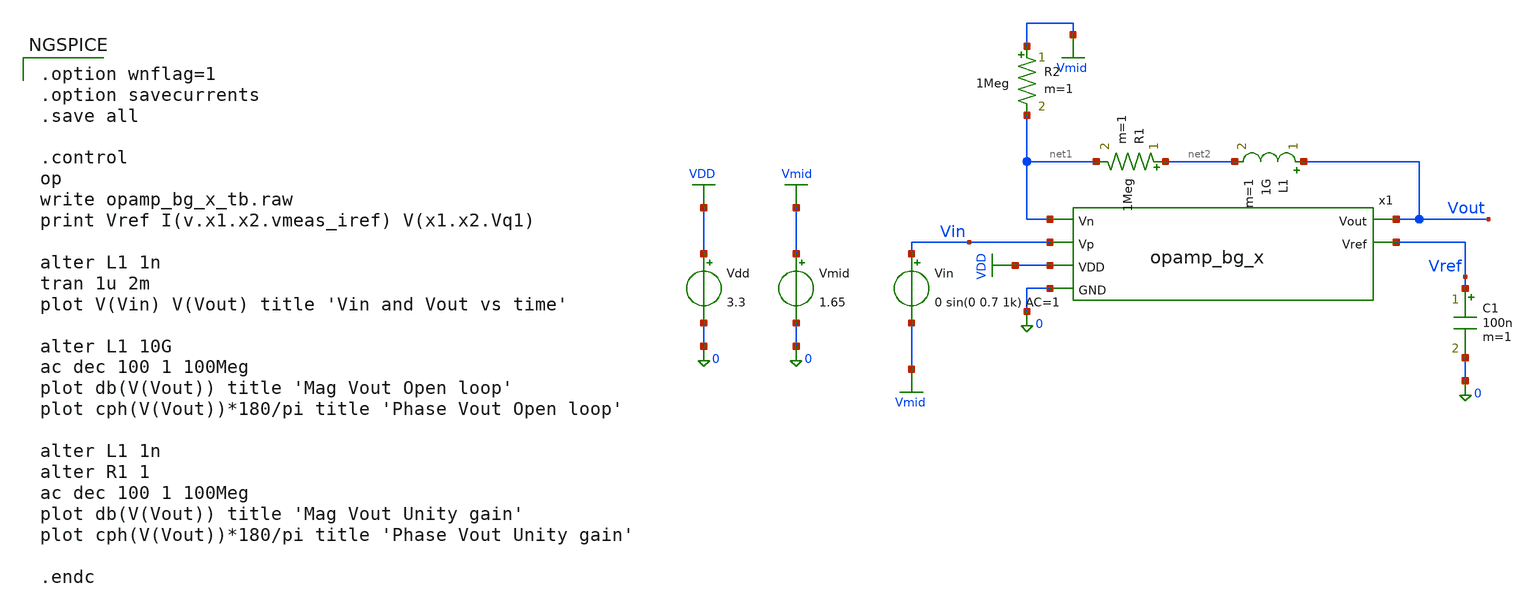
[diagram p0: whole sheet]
** sch_path: xschem/opamp_bg_x_tb.sch
**.subckt opamp_bg_x_tb
x1 Vref net1 Vout Vin VDD 0 opamp_bg_x
R1 net2 net1 1Meg m=1
L1 Vout net2 1G m=1
R2 Vmid net1 1Meg m=1
Vin Vin Vmid 0 sin(0 0.7 1k) AC=1
Vmid Vmid 0 1.65
Vdd VDD 0 3.3
C1 Vref 0 100n m=1
**** begin user architecture code

.option wnflag=1
.option savecurrents
.save all

.control
op
write opamp_bg_x_tb.raw
print Vref I(v.x1.x2.vmeas_iref) V(x1.x2.Vq1)

alter L1 1n
tran 1u 2m
plot V(Vin) V(Vout) title 'Vin and Vout vs time'

alter L1 10G
ac dec 100 1 100Meg
plot db(V(Vout)) title 'Mag Vout Open loop'
plot cph(V(Vout))*180/pi title 'Phase Vout Open loop'

alter L1 1n
alter R1 1
ac dec 100 1 100Meg
plot db(V(Vout)) title 'Mag Vout Unity gain'
plot cph(V(Vout))*180/pi title 'Phase Vout Unity gain'

.endc


** opencircuitdesign pdks install
.lib $::SKYWATER_MODELS/sky130.lib.spice tt

**** end user architecture code
**.ends

* expanding   symbol:  opamp_bg_x.sym # of pins=6
** sym_path: xschem/opamp_bg_x.sym
** sch_path: xschem/opamp_bg_x.sch
.subckt opamp_bg_x Vref Vn Vout Vp VDD GND
*.ipin Vn
*.opin Vout
*.opin Vref
*.ipin Vp
*.ipin VDD
*.ipin GND
x1 VDD Vref GND bandgap_x
x2 VDD Vp Vn Vout Vref GND opamp_x
.ends


* expanding   symbol:  /home/bbarkey/Documents/ECE_5120/homework_05/xschem/bandgap_x.sym # of pins=3
** sym_path: xschem/bandgap_x.sym
** sch_path: xschem/bandgap_x.sch
.subckt bandgap_x VDD Vref GND
*.opin Vref
*.ipin GND
*.ipin VDD
XM2 Vg3 Vg2 net1 net1 sky130_fd_pr__pfet_g5v0d10v5 L=1 W=20 nf=1 ad='int((1 + 1)/2) * 20 / 1 * 0.29'
+ as='int((1 + 2)/2) * 20 / 1 * 0.29' pd='2*int((1 + 1)/2) * (20 / 1 + 0.29)' ps='2*int((1 + 2)/2) * (20 / 1 + 0.29)'
+ nrd='0.29 / 20 ' nrs='0.29 / 20 ' sa=0 sb=0 sd=0 mult=1 m=1
XM1 Vg10 Vg1 net1 net1 sky130_fd_pr__pfet_g5v0d10v5 L=1 W=20 nf=1 ad='int((1 + 1)/2) * 20 / 1 * 0.29'
+ as='int((1 + 2)/2) * 20 / 1 * 0.29' pd='2*int((1 + 1)/2) * (20 / 1 + 0.29)' ps='2*int((1 + 2)/2) * (20 / 1 + 0.29)'
+ nrd='0.29 / 20 ' nrs='0.29 / 20 ' sa=0 sb=0 sd=0 mult=1 m=1
XM3 Vg10 Vg3 GND GND sky130_fd_pr__nfet_g5v0d10v5 L=1 W=20 nf=1 ad='int((1 + 1)/2) * 20 / 1 * 0.29' as='int((1 + 2)/2) * 20 / 1 * 0.29'
+ pd='2*int((1 + 1)/2) * (20 / 1 + 0.29)' ps='2*int((1 + 2)/2) * (20 / 1 + 0.29)' nrd='0.29 / 20 ' nrs='0.29 / 20 '
+ sa=0 sb=0 sd=0 mult=1 m=1
XM4 Vg3 Vg3 GND GND sky130_fd_pr__nfet_g5v0d10v5 L=1 W=20 nf=1 ad='int((1 + 1)/2) * 20 / 1 * 0.29' as='int((1 + 2)/2) * 20 / 1 * 0.29'
+ pd='2*int((1 + 1)/2) * (20 / 1 + 0.29)' ps='2*int((1 + 2)/2) * (20 / 1 + 0.29)' nrd='0.29 / 20 ' nrs='0.29 / 20 '
+ sa=0 sb=0 sd=0 mult=1 m=1
XM5 Vg5 Vg5 VDD VDD sky130_fd_pr__pfet_g5v0d10v5 L=1 W=1 nf=1 ad='int((1 + 1)/2) * 1 / 1 * 0.29' as='int((1 + 2)/2) * 1 / 1 * 0.29'
+ pd='2*int((1 + 1)/2) * (1 / 1 + 0.29)' ps='2*int((1 + 2)/2) * (1 / 1 + 0.29)' nrd='0.29 / 1 ' nrs='0.29 / 1 '
+ sa=0 sb=0 sd=0 mult=1 m=1
XM6 Vg5 Vref Vs5 GND sky130_fd_pr__nfet_g5v0d10v5 L=1 W=5 nf=1 ad='int((1 + 1)/2) * 5 / 1 * 0.29' as='int((1 + 2)/2) * 5 / 1 * 0.29'
+ pd='2*int((1 + 1)/2) * (5 / 1 + 0.29)' ps='2*int((1 + 2)/2) * (5 / 1 + 0.29)' nrd='0.29 / 5 ' nrs='0.29 / 5 '
+ sa=0 sb=0 sd=0 mult=1 m=1
XM7a Vg12 Vg12 net3 GND sky130_fd_pr__nfet_g5v0d10v5 L=10 W=0.5 nf=1 ad='int((1 + 1)/2) * 0.5 / 1 * 0.29'
+ as='int((1 + 2)/2) * 0.5 / 1 * 0.29' pd='2*int((1 + 1)/2) * (0.5 / 1 + 0.29)' ps='2*int((1 + 2)/2) * (0.5 / 1 + 0.29)'
+ nrd='0.29 / 0.5 ' nrs='0.29 / 0.5 ' sa=0 sb=0 sd=0 mult=1 m=1
XM8 Vg12 Vg5 VDD VDD sky130_fd_pr__pfet_g5v0d10v5 L=1 W=1 nf=1 ad='int((1 + 1)/2) * 1 / 1 * 0.29' as='int((1 + 2)/2) * 1 / 1 * 0.29'
+ pd='2*int((1 + 1)/2) * (1 / 1 + 0.29)' ps='2*int((1 + 2)/2) * (1 / 1 + 0.29)' nrd='0.29 / 1 ' nrs='0.29 / 1 '
+ sa=0 sb=0 sd=0 mult=1 m=1
XM9 Vg12 Vref net2 GND sky130_fd_pr__nfet_g5v0d10v5 L=1 W=20 nf=1 ad='int((1 + 1)/2) * 20 / 1 * 0.29'
+ as='int((1 + 2)/2) * 20 / 1 * 0.29' pd='2*int((1 + 1)/2) * (20 / 1 + 0.29)' ps='2*int((1 + 2)/2) * (20 / 1 + 0.29)'
+ nrd='0.29 / 20 ' nrs='0.29 / 20 ' sa=0 sb=0 sd=0 mult=1 m=1
XM10 net2 Vg10 GND GND sky130_fd_pr__nfet_g5v0d10v5 L=1 W=20 nf=1 ad='int((1 + 1)/2) * 20 / 1 * 0.29'
+ as='int((1 + 2)/2) * 20 / 1 * 0.29' pd='2*int((1 + 1)/2) * (20 / 1 + 0.29)' ps='2*int((1 + 2)/2) * (20 / 1 + 0.29)'
+ nrd='0.29 / 20 ' nrs='0.29 / 20 ' sa=0 sb=0 sd=0 mult=1 m=1
XM11 net1 Vg5 VDD VDD sky130_fd_pr__pfet_g5v0d10v5 L=1 W=1 nf=1 ad='int((1 + 1)/2) * 1 / 1 * 0.29' as='int((1 + 2)/2) * 1 / 1 * 0.29'
+ pd='2*int((1 + 1)/2) * (1 / 1 + 0.29)' ps='2*int((1 + 2)/2) * (1 / 1 + 0.29)' nrd='0.29 / 1 ' nrs='0.29 / 1 '
+ sa=0 sb=0 sd=0 mult=1 m=1
XM12 Vref Vg12 VDD VDD sky130_fd_pr__pfet_g5v0d10v5 L=0.5 W=20 nf=1 ad='int((1 + 1)/2) * 20 / 1 * 0.29'
+ as='int((1 + 2)/2) * 20 / 1 * 0.29' pd='2*int((1 + 1)/2) * (20 / 1 + 0.29)' ps='2*int((1 + 2)/2) * (20 / 1 + 0.29)'
+ nrd='0.29 / 20 ' nrs='0.29 / 20 ' sa=0 sb=0 sd=0 mult=1 m=1
XR1 Vg2 Vref GND sky130_fd_pr__res_high_po_0p35 L=21.3 mult=1 m=1
XR2 Vg1 Vref GND sky130_fd_pr__res_high_po_0p35 L=21.3 mult=1 m=1
XR3 Ve1 Vg1 GND sky130_fd_pr__res_high_po_0p35 L=3 mult=1 m=1
XR4 GND Vs5 GND sky130_fd_pr__res_high_po_0p35 L=47.02 mult=1 m=1
XQ1 GND GND Ve1 sky130_fd_pr__pnp_05v5_W3p40L3p40 m=24
XQ2 GND GND Vg2 sky130_fd_pr__pnp_05v5_W3p40L3p40 m=1
XM7b net3 Vg12 net4 GND sky130_fd_pr__nfet_g5v0d10v5 L=10 W=0.5 nf=1 ad='int((1 + 1)/2) * 0.5 / 1 * 0.29'
+ as='int((1 + 2)/2) * 0.5 / 1 * 0.29' pd='2*int((1 + 1)/2) * (0.5 / 1 + 0.29)' ps='2*int((1 + 2)/2) * (0.5 / 1 + 0.29)'
+ nrd='0.29 / 0.5 ' nrs='0.29 / 0.5 ' sa=0 sb=0 sd=0 mult=1 m=1
XM7c net4 Vg12 net5 GND sky130_fd_pr__nfet_g5v0d10v5 L=10 W=0.5 nf=1 ad='int((1 + 1)/2) * 0.5 / 1 * 0.29'
+ as='int((1 + 2)/2) * 0.5 / 1 * 0.29' pd='2*int((1 + 1)/2) * (0.5 / 1 + 0.29)' ps='2*int((1 + 2)/2) * (0.5 / 1 + 0.29)'
+ nrd='0.29 / 0.5 ' nrs='0.29 / 0.5 ' sa=0 sb=0 sd=0 mult=1 m=1
XM7d net5 Vg12 net6 GND sky130_fd_pr__nfet_g5v0d10v5 L=10 W=0.5 nf=1 ad='int((1 + 1)/2) * 0.5 / 1 * 0.29'
+ as='int((1 + 2)/2) * 0.5 / 1 * 0.29' pd='2*int((1 + 1)/2) * (0.5 / 1 + 0.29)' ps='2*int((1 + 2)/2) * (0.5 / 1 + 0.29)'
+ nrd='0.29 / 0.5 ' nrs='0.29 / 0.5 ' sa=0 sb=0 sd=0 mult=1 m=1
XM7e net6 Vg12 net7 GND sky130_fd_pr__nfet_g5v0d10v5 L=10 W=0.5 nf=1 ad='int((1 + 1)/2) * 0.5 / 1 * 0.29'
+ as='int((1 + 2)/2) * 0.5 / 1 * 0.29' pd='2*int((1 + 1)/2) * (0.5 / 1 + 0.29)' ps='2*int((1 + 2)/2) * (0.5 / 1 + 0.29)'
+ nrd='0.29 / 0.5 ' nrs='0.29 / 0.5 ' sa=0 sb=0 sd=0 mult=1 m=1
XM7 net7 Vg12 net8 GND sky130_fd_pr__nfet_g5v0d10v5 L=10 W=0.5 nf=1 ad='int((1 + 1)/2) * 0.5 / 1 * 0.29'
+ as='int((1 + 2)/2) * 0.5 / 1 * 0.29' pd='2*int((1 + 1)/2) * (0.5 / 1 + 0.29)' ps='2*int((1 + 2)/2) * (0.5 / 1 + 0.29)'
+ nrd='0.29 / 0.5 ' nrs='0.29 / 0.5 ' sa=0 sb=0 sd=0 mult=1 m=1
XM13 net8 Vg12 net9 GND sky130_fd_pr__nfet_g5v0d10v5 L=10 W=0.5 nf=1 ad='int((1 + 1)/2) * 0.5 / 1 * 0.29'
+ as='int((1 + 2)/2) * 0.5 / 1 * 0.29' pd='2*int((1 + 1)/2) * (0.5 / 1 + 0.29)' ps='2*int((1 + 2)/2) * (0.5 / 1 + 0.29)'
+ nrd='0.29 / 0.5 ' nrs='0.29 / 0.5 ' sa=0 sb=0 sd=0 mult=1 m=1
XM14 net9 Vg12 net10 GND sky130_fd_pr__nfet_g5v0d10v5 L=10 W=0.5 nf=1 ad='int((1 + 1)/2) * 0.5 / 1 * 0.29'
+ as='int((1 + 2)/2) * 0.5 / 1 * 0.29' pd='2*int((1 + 1)/2) * (0.5 / 1 + 0.29)' ps='2*int((1 + 2)/2) * (0.5 / 1 + 0.29)'
+ nrd='0.29 / 0.5 ' nrs='0.29 / 0.5 ' sa=0 sb=0 sd=0 mult=1 m=1
XM15 net10 Vg12 net11 GND sky130_fd_pr__nfet_g5v0d10v5 L=10 W=0.5 nf=1 ad='int((1 + 1)/2) * 0.5 / 1 * 0.29'
+ as='int((1 + 2)/2) * 0.5 / 1 * 0.29' pd='2*int((1 + 1)/2) * (0.5 / 1 + 0.29)' ps='2*int((1 + 2)/2) * (0.5 / 1 + 0.29)'
+ nrd='0.29 / 0.5 ' nrs='0.29 / 0.5 ' sa=0 sb=0 sd=0 mult=1 m=1
XM16 net11 Vg12 GND GND sky130_fd_pr__nfet_g5v0d10v5 L=10 W=0.5 nf=1 ad='int((1 + 1)/2) * 0.5 / 1 * 0.29'
+ as='int((1 + 2)/2) * 0.5 / 1 * 0.29' pd='2*int((1 + 1)/2) * (0.5 / 1 + 0.29)' ps='2*int((1 + 2)/2) * (0.5 / 1 + 0.29)'
+ nrd='0.29 / 0.5 ' nrs='0.29 / 0.5 ' sa=0 sb=0 sd=0 mult=1 m=1
.ends


* expanding   symbol:  opamp_x.sym # of pins=6
** sym_path: xschem/opamp_x.sym
** sch_path: xschem/opamp_x.sch
.subckt opamp_x VDD Vp Vn Vout Vref GND
*.ipin Vref
*.ipin Vn
*.ipin Vp
*.opin Vout
*.ipin VDD
*.ipin GND
XM1 net3 net3 net1 GND sky130_fd_pr__nfet_g5v0d10v5 L=2 W=3.33 nf=1 ad='int((1 + 1)/2) * 3.33 / 1 * 0.29'
+ as='int((1 + 2)/2) * 3.33 / 1 * 0.29' pd='2*int((1 + 1)/2) * (3.33 / 1 + 0.29)' ps='2*int((1 + 2)/2) * (3.33 / 1 + 0.29)'
+ nrd='0.29 / 3.33 ' nrs='0.29 / 3.33 ' sa=0 sb=0 sd=0 mult=3 m=3
XM2 net1 net3 GND GND sky130_fd_pr__nfet_g5v0d10v5 L=5 W=5 nf=1 ad='int((1 + 1)/2) * 5 / 1 * 0.29' as='int((1 + 2)/2) * 5 / 1 * 0.29'
+ pd='2*int((1 + 1)/2) * (5 / 1 + 0.29)' ps='2*int((1 + 2)/2) * (5 / 1 + 0.29)' nrd='0.29 / 5 ' nrs='0.29 / 5 '
+ sa=0 sb=0 sd=0 mult=1 m=1
XM3 net2 net3 net4 GND sky130_fd_pr__nfet_g5v0d10v5 L=2 W=3.33 nf=1 ad='int((1 + 1)/2) * 3.33 / 1 * 0.29'
+ as='int((1 + 2)/2) * 3.33 / 1 * 0.29' pd='2*int((1 + 1)/2) * (3.33 / 1 + 0.29)' ps='2*int((1 + 2)/2) * (3.33 / 1 + 0.29)'
+ nrd='0.29 / 3.33 ' nrs='0.29 / 3.33 ' sa=0 sb=0 sd=0 mult=3 m=3
XM4 net4 net3 GND GND sky130_fd_pr__nfet_g5v0d10v5 L=5 W=5 nf=1 ad='int((1 + 1)/2) * 5 / 1 * 0.29' as='int((1 + 2)/2) * 5 / 1 * 0.29'
+ pd='2*int((1 + 1)/2) * (5 / 1 + 0.29)' ps='2*int((1 + 2)/2) * (5 / 1 + 0.29)' nrd='0.29 / 5 ' nrs='0.29 / 5 '
+ sa=0 sb=0 sd=0 mult=1 m=1
XM5 net5 net2 VDD VDD sky130_fd_pr__pfet_g5v0d10v5 L=1 W=3 nf=1 ad='int((1 + 1)/2) * 3 / 1 * 0.29' as='int((1 + 2)/2) * 3 / 1 * 0.29'
+ pd='2*int((1 + 1)/2) * (3 / 1 + 0.29)' ps='2*int((1 + 2)/2) * (3 / 1 + 0.29)' nrd='0.29 / 3 ' nrs='0.29 / 3 '
+ sa=0 sb=0 sd=0 mult=1 m=1
XM6 net2 net2 net5 VDD sky130_fd_pr__pfet_g5v0d10v5 L=1 W=10 nf=1 ad='int((1 + 1)/2) * 10 / 1 * 0.29'
+ as='int((1 + 2)/2) * 10 / 1 * 0.29' pd='2*int((1 + 1)/2) * (10 / 1 + 0.29)' ps='2*int((1 + 2)/2) * (10 / 1 + 0.29)'
+ nrd='0.29 / 10 ' nrs='0.29 / 10 ' sa=0 sb=0 sd=0 mult=1 m=1
XM7 net6 net2 VDD VDD sky130_fd_pr__pfet_g5v0d10v5 L=1 W=1 nf=1 ad='int((1 + 1)/2) * 1 / 1 * 0.29' as='int((1 + 2)/2) * 1 / 1 * 0.29'
+ pd='2*int((1 + 1)/2) * (1 / 1 + 0.29)' ps='2*int((1 + 2)/2) * (1 / 1 + 0.29)' nrd='0.29 / 1 ' nrs='0.29 / 1 '
+ sa=0 sb=0 sd=0 mult=3 m=3
XM8 net7 net2 net6 VDD sky130_fd_pr__pfet_g5v0d10v5 L=0.5 W=10 nf=1 ad='int((1 + 1)/2) * 10 / 1 * 0.29'
+ as='int((1 + 2)/2) * 10 / 1 * 0.29' pd='2*int((1 + 1)/2) * (10 / 1 + 0.29)' ps='2*int((1 + 2)/2) * (10 / 1 + 0.29)'
+ nrd='0.29 / 10 ' nrs='0.29 / 10 ' sa=0 sb=0 sd=0 mult=1 m=1
XM9 net13 Vp net7 VDD sky130_fd_pr__pfet_g5v0d10v5 L=3 W=20 nf=1 ad='int((1 + 1)/2) * 20 / 1 * 0.29'
+ as='int((1 + 2)/2) * 20 / 1 * 0.29' pd='2*int((1 + 1)/2) * (20 / 1 + 0.29)' ps='2*int((1 + 2)/2) * (20 / 1 + 0.29)'
+ nrd='0.29 / 20 ' nrs='0.29 / 20 ' sa=0 sb=0 sd=0 mult=10 m=10
XM10 net12 Vn net7 VDD sky130_fd_pr__pfet_g5v0d10v5 L=3 W=20 nf=1 ad='int((1 + 1)/2) * 20 / 1 * 0.29'
+ as='int((1 + 2)/2) * 20 / 1 * 0.29' pd='2*int((1 + 1)/2) * (20 / 1 + 0.29)' ps='2*int((1 + 2)/2) * (20 / 1 + 0.29)'
+ nrd='0.29 / 20 ' nrs='0.29 / 20 ' sa=0 sb=0 sd=0 mult=10 m=10
XM11 net10 net9 VDD VDD sky130_fd_pr__pfet_g5v0d10v5 L=0.5 W=2 nf=1 ad='int((1 + 1)/2) * 2 / 1 * 0.29'
+ as='int((1 + 2)/2) * 2 / 1 * 0.29' pd='2*int((1 + 1)/2) * (2 / 1 + 0.29)' ps='2*int((1 + 2)/2) * (2 / 1 + 0.29)'
+ nrd='0.29 / 2 ' nrs='0.29 / 2 ' sa=0 sb=0 sd=0 mult=5 m=5
XM12 net9 net9 net10 VDD sky130_fd_pr__pfet_g5v0d10v5 L=0.5 W=5 nf=1 ad='int((1 + 1)/2) * 5 / 1 * 0.29'
+ as='int((1 + 2)/2) * 5 / 1 * 0.29' pd='2*int((1 + 1)/2) * (5 / 1 + 0.29)' ps='2*int((1 + 2)/2) * (5 / 1 + 0.29)'
+ nrd='0.29 / 5 ' nrs='0.29 / 5 ' sa=0 sb=0 sd=0 mult=5 m=5
XM13 net11 net9 VDD VDD sky130_fd_pr__pfet_g5v0d10v5 L=0.5 W=2 nf=1 ad='int((1 + 1)/2) * 2 / 1 * 0.29'
+ as='int((1 + 2)/2) * 2 / 1 * 0.29' pd='2*int((1 + 1)/2) * (2 / 1 + 0.29)' ps='2*int((1 + 2)/2) * (2 / 1 + 0.29)'
+ nrd='0.29 / 2 ' nrs='0.29 / 2 ' sa=0 sb=0 sd=0 mult=5 m=5
XM14 net18 net9 net11 VDD sky130_fd_pr__pfet_g5v0d10v5 L=0.5 W=5 nf=1 ad='int((1 + 1)/2) * 5 / 1 * 0.29'
+ as='int((1 + 2)/2) * 5 / 1 * 0.29' pd='2*int((1 + 1)/2) * (5 / 1 + 0.29)' ps='2*int((1 + 2)/2) * (5 / 1 + 0.29)'
+ nrd='0.29 / 5 ' nrs='0.29 / 5 ' sa=0 sb=0 sd=0 mult=5 m=5
XM15 net9 net3 net12 GND sky130_fd_pr__nfet_g5v0d10v5 L=0.5 W=5 nf=1 ad='int((1 + 1)/2) * 5 / 1 * 0.29'
+ as='int((1 + 2)/2) * 5 / 1 * 0.29' pd='2*int((1 + 1)/2) * (5 / 1 + 0.29)' ps='2*int((1 + 2)/2) * (5 / 1 + 0.29)'
+ nrd='0.29 / 5 ' nrs='0.29 / 5 ' sa=0 sb=0 sd=0 mult=5 m=5
XM16 net12 net3 GND GND sky130_fd_pr__nfet_g5v0d10v5 L=0.5 W=1 nf=1 ad='int((1 + 1)/2) * 1 / 1 * 0.29'
+ as='int((1 + 2)/2) * 1 / 1 * 0.29' pd='2*int((1 + 1)/2) * (1 / 1 + 0.29)' ps='2*int((1 + 2)/2) * (1 / 1 + 0.29)'
+ nrd='0.29 / 1 ' nrs='0.29 / 1 ' sa=0 sb=0 sd=0 mult=1 m=1
XM17 net17 net3 net13 GND sky130_fd_pr__nfet_g5v0d10v5 L=0.5 W=5 nf=1 ad='int((1 + 1)/2) * 5 / 1 * 0.29'
+ as='int((1 + 2)/2) * 5 / 1 * 0.29' pd='2*int((1 + 1)/2) * (5 / 1 + 0.29)' ps='2*int((1 + 2)/2) * (5 / 1 + 0.29)'
+ nrd='0.29 / 5 ' nrs='0.29 / 5 ' sa=0 sb=0 sd=0 mult=5 m=5
XM18 net13 net3 GND GND sky130_fd_pr__nfet_g5v0d10v5 L=0.5 W=1 nf=1 ad='int((1 + 1)/2) * 1 / 1 * 0.29'
+ as='int((1 + 2)/2) * 1 / 1 * 0.29' pd='2*int((1 + 1)/2) * (1 / 1 + 0.29)' ps='2*int((1 + 2)/2) * (1 / 1 + 0.29)'
+ nrd='0.29 / 1 ' nrs='0.29 / 1 ' sa=0 sb=0 sd=0 mult=1 m=1
XM19 net17 net14 net18 VDD sky130_fd_pr__pfet_g5v0d10v5 L=0.5 W=5.55 nf=1 ad='int((1 + 1)/2) * 5.55 / 1 * 0.29'
+ as='int((1 + 2)/2) * 5.55 / 1 * 0.29' pd='2*int((1 + 1)/2) * (5.55 / 1 + 0.29)' ps='2*int((1 + 2)/2) * (5.55 / 1 + 0.29)'
+ nrd='0.29 / 5.55 ' nrs='0.29 / 5.55 ' sa=0 sb=0 sd=0 mult=9 m=9
XM20 net14 net3 GND GND sky130_fd_pr__nfet_g5v0d10v5 L=1.67 W=0.5 nf=1 ad='int((1 + 1)/2) * 0.5 / 1 * 0.29'
+ as='int((1 + 2)/2) * 0.5 / 1 * 0.29' pd='2*int((1 + 1)/2) * (0.5 / 1 + 0.29)' ps='2*int((1 + 2)/2) * (0.5 / 1 + 0.29)'
+ nrd='0.29 / 0.5 ' nrs='0.29 / 0.5 ' sa=0 sb=0 sd=0 mult=1 m=1
XM21 net15 net15 VDD VDD sky130_fd_pr__pfet_g5v0d10v5 L=1 W=1.67 nf=1 ad='int((1 + 1)/2) * 1.67 / 1 * 0.29'
+ as='int((1 + 2)/2) * 1.67 / 1 * 0.29' pd='2*int((1 + 1)/2) * (1.67 / 1 + 0.29)' ps='2*int((1 + 2)/2) * (1.67 / 1 + 0.29)'
+ nrd='0.29 / 1.67 ' nrs='0.29 / 1.67 ' sa=0 sb=0 sd=0 mult=9 m=9
XM22 net14 net14 net15 VDD sky130_fd_pr__pfet_g5v0d10v5 L=1 W=1.67 nf=1 ad='int((1 + 1)/2) * 1.67 / 1 * 0.29'
+ as='int((1 + 2)/2) * 1.67 / 1 * 0.29' pd='2*int((1 + 1)/2) * (1.67 / 1 + 0.29)' ps='2*int((1 + 2)/2) * (1.67 / 1 + 0.29)'
+ nrd='0.29 / 1.67 ' nrs='0.29 / 1.67 ' sa=0 sb=0 sd=0 mult=9 m=9
XM24 net16 net2 VDD VDD sky130_fd_pr__pfet_g5v0d10v5 L=1 W=0.8 nf=1 ad='int((1 + 1)/2) * 0.8 / 1 * 0.29'
+ as='int((1 + 2)/2) * 0.8 / 1 * 0.29' pd='2*int((1 + 1)/2) * (0.8 / 1 + 0.29)' ps='2*int((1 + 2)/2) * (0.8 / 1 + 0.29)'
+ nrd='0.29 / 0.8 ' nrs='0.29 / 0.8 ' sa=0 sb=0 sd=0 mult=1 m=1
XM25 net16 net16 net19 GND sky130_fd_pr__nfet_g5v0d10v5 L=0.5 W=7 nf=1 ad='int((1 + 1)/2) * 7 / 1 * 0.29'
+ as='int((1 + 2)/2) * 7 / 1 * 0.29' pd='2*int((1 + 1)/2) * (7 / 1 + 0.29)' ps='2*int((1 + 2)/2) * (7 / 1 + 0.29)'
+ nrd='0.29 / 7 ' nrs='0.29 / 7 ' sa=0 sb=0 sd=0 mult=15 m=15
XM26 net19 net19 GND GND sky130_fd_pr__nfet_g5v0d10v5 L=0.5 W=7 nf=1 ad='int((1 + 1)/2) * 7 / 1 * 0.29'
+ as='int((1 + 2)/2) * 7 / 1 * 0.29' pd='2*int((1 + 1)/2) * (7 / 1 + 0.29)' ps='2*int((1 + 2)/2) * (7 / 1 + 0.29)'
+ nrd='0.29 / 7 ' nrs='0.29 / 7 ' sa=0 sb=0 sd=0 mult=15 m=15
XM27 Vout net18 VDD VDD sky130_fd_pr__pfet_g5v0d10v5 L=0.5 W=3 nf=1 ad='int((1 + 1)/2) * 3 / 1 * 0.29'
+ as='int((1 + 2)/2) * 3 / 1 * 0.29' pd='2*int((1 + 1)/2) * (3 / 1 + 0.29)' ps='2*int((1 + 2)/2) * (3 / 1 + 0.29)'
+ nrd='0.29 / 3 ' nrs='0.29 / 3 ' sa=0 sb=0 sd=0 mult=5 m=5
XM28 Vout net17 GND GND sky130_fd_pr__nfet_g5v0d10v5 L=0.5 W=3 nf=1 ad='int((1 + 1)/2) * 3 / 1 * 0.29'
+ as='int((1 + 2)/2) * 3 / 1 * 0.29' pd='2*int((1 + 1)/2) * (3 / 1 + 0.29)' ps='2*int((1 + 2)/2) * (3 / 1 + 0.29)'
+ nrd='0.29 / 3 ' nrs='0.29 / 3 ' sa=0 sb=0 sd=0 mult=5 m=5
XM33 net11 Vp net8 GND sky130_fd_pr__nfet_g5v0d10v5 L=2 W=20 nf=1 ad='int((1 + 1)/2) * 20 / 1 * 0.29'
+ as='int((1 + 2)/2) * 20 / 1 * 0.29' pd='2*int((1 + 1)/2) * (20 / 1 + 0.29)' ps='2*int((1 + 2)/2) * (20 / 1 + 0.29)'
+ nrd='0.29 / 20 ' nrs='0.29 / 20 ' sa=0 sb=0 sd=0 mult=5 m=5
XM30 net10 Vn net8 GND sky130_fd_pr__nfet_g5v0d10v5 L=2 W=20 nf=1 ad='int((1 + 1)/2) * 20 / 1 * 0.29'
+ as='int((1 + 2)/2) * 20 / 1 * 0.29' pd='2*int((1 + 1)/2) * (20 / 1 + 0.29)' ps='2*int((1 + 2)/2) * (20 / 1 + 0.29)'
+ nrd='0.29 / 20 ' nrs='0.29 / 20 ' sa=0 sb=0 sd=0 mult=5 m=5
XM31 net8 net3 net22 GND sky130_fd_pr__nfet_g5v0d10v5 L=1 W=3.33 nf=1 ad='int((1 + 1)/2) * 3.33 / 1 * 0.29'
+ as='int((1 + 2)/2) * 3.33 / 1 * 0.29' pd='2*int((1 + 1)/2) * (3.33 / 1 + 0.29)' ps='2*int((1 + 2)/2) * (3.33 / 1 + 0.29)'
+ nrd='0.29 / 3.33 ' nrs='0.29 / 3.33 ' sa=0 sb=0 sd=0 mult=3 m=3
XM32 net22 net3 GND GND sky130_fd_pr__nfet_g5v0d10v5 L=0.5 W=1 nf=1 ad='int((1 + 1)/2) * 1 / 1 * 0.29'
+ as='int((1 + 2)/2) * 1 / 1 * 0.29' pd='2*int((1 + 1)/2) * (1 / 1 + 0.29)' ps='2*int((1 + 2)/2) * (1 / 1 + 0.29)'
+ nrd='0.29 / 1 ' nrs='0.29 / 1 ' sa=0 sb=0 sd=0 mult=1 m=1
XM23 net18 net16 net17 GND sky130_fd_pr__nfet_g5v0d10v5 L=0.5 W=5.55 nf=1 ad='int((1 + 1)/2) * 5.55 / 1 * 0.29'
+ as='int((1 + 2)/2) * 5.55 / 1 * 0.29' pd='2*int((1 + 1)/2) * (5.55 / 1 + 0.29)' ps='2*int((1 + 2)/2) * (5.55 / 1 + 0.29)'
+ nrd='0.29 / 5.55 ' nrs='0.29 / 5.55 ' sa=0 sb=0 sd=0 mult=9 m=9
XMr1 net21 Vref GND GND sky130_fd_pr__nfet_g5v0d10v5 L=1.75 W=1.25 nf=1 ad='int((1 + 1)/2) * 1.25 / 1 * 0.29'
+ as='int((1 + 2)/2) * 1.25 / 1 * 0.29' pd='2*int((1 + 1)/2) * (1.25 / 1 + 0.29)' ps='2*int((1 + 2)/2) * (1.25 / 1 + 0.29)'
+ nrd='0.29 / 1.25 ' nrs='0.29 / 1.25 ' sa=0 sb=0 sd=0 mult=1 m=1
XMr2 net20 net20 VDD VDD sky130_fd_pr__pfet_g5v0d10v5 L=1 W=1 nf=1 ad='int((1 + 1)/2) * 1 / 1 * 0.29'
+ as='int((1 + 2)/2) * 1 / 1 * 0.29' pd='2*int((1 + 1)/2) * (1 / 1 + 0.29)' ps='2*int((1 + 2)/2) * (1 / 1 + 0.29)'
+ nrd='0.29 / 1 ' nrs='0.29 / 1 ' sa=0 sb=0 sd=0 mult=1 m=1
XMr3 net3 net20 VDD VDD sky130_fd_pr__pfet_g5v0d10v5 L=1 W=1 nf=1 ad='int((1 + 1)/2) * 1 / 1 * 0.29'
+ as='int((1 + 2)/2) * 1 / 1 * 0.29' pd='2*int((1 + 1)/2) * (1 / 1 + 0.29)' ps='2*int((1 + 2)/2) * (1 / 1 + 0.29)'
+ nrd='0.29 / 1 ' nrs='0.29 / 1 ' sa=0 sb=0 sd=0 mult=1 m=1
Vmeas_Iref net20 net21 0
.save i(vmeas_iref)
XC2 Vout net17 sky130_fd_pr__cap_mim_m3_2 W=25 L=25 MF=4 m=4
XC1 net18 Vout sky130_fd_pr__cap_mim_m3_2 W=25 L=25 MF=4 m=4
.ends

.GLOBAL Vmid
.GLOBAL VDD
.end
